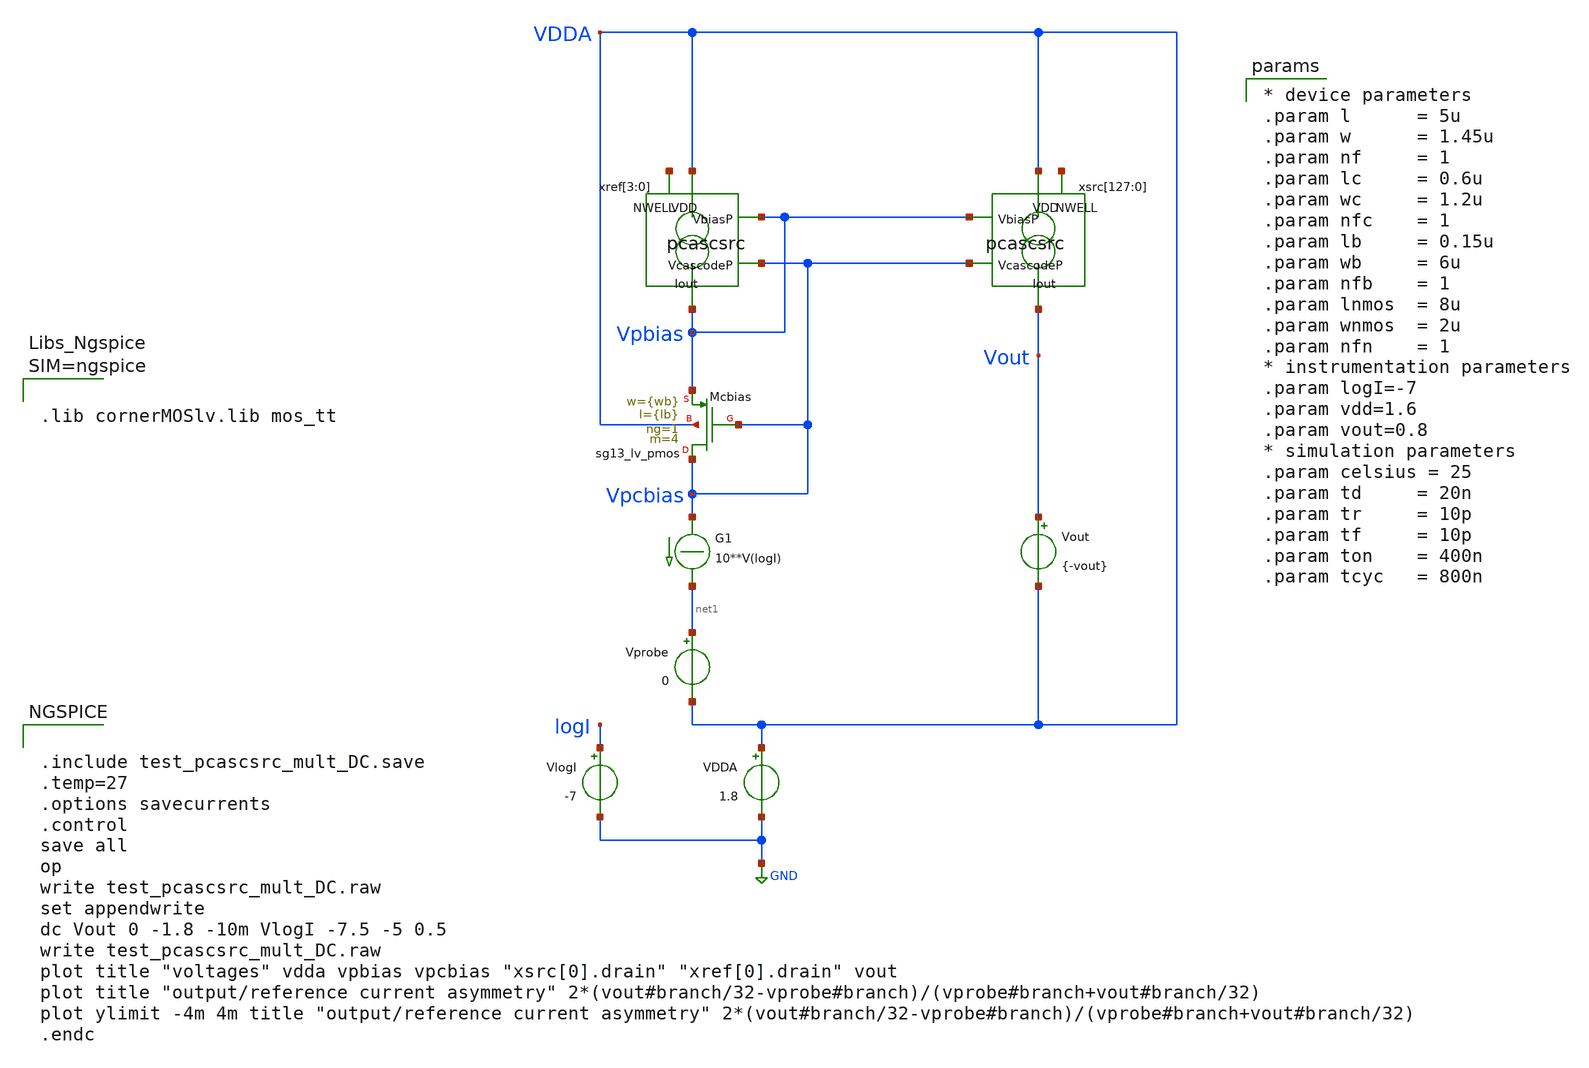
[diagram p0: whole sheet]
** sch_path: xschem/test_pcascsrc_mult_DC.sch
**.subckt test_pcascsrc_mult_DC
Vout Vout VDDA {-vout}
.save i(vout)
Vprobe net1 VDDA 0
.save i(vprobe)
G1 Vpcbias net1 CUR=' 10**V(logI) '
VlogI logI GND -7
.save i(vlogi)
xref[3] VDDA Vpbias Vpcbias Vpbias net2[3] pcascsrc
xref[2] VDDA Vpbias Vpcbias Vpbias net2[2] pcascsrc
xref[1] VDDA Vpbias Vpcbias Vpbias net2[1] pcascsrc
xref[0] VDDA Vpbias Vpcbias Vpbias net2[0] pcascsrc
xsrc[127] VDDA Vpbias Vpcbias Vout net3[127] pcascsrc
xsrc[126] VDDA Vpbias Vpcbias Vout net3[126] pcascsrc
xsrc[125] VDDA Vpbias Vpcbias Vout net3[125] pcascsrc
xsrc[124] VDDA Vpbias Vpcbias Vout net3[124] pcascsrc
xsrc[123] VDDA Vpbias Vpcbias Vout net3[123] pcascsrc
xsrc[122] VDDA Vpbias Vpcbias Vout net3[122] pcascsrc
xsrc[121] VDDA Vpbias Vpcbias Vout net3[121] pcascsrc
xsrc[120] VDDA Vpbias Vpcbias Vout net3[120] pcascsrc
xsrc[119] VDDA Vpbias Vpcbias Vout net3[119] pcascsrc
xsrc[118] VDDA Vpbias Vpcbias Vout net3[118] pcascsrc
xsrc[117] VDDA Vpbias Vpcbias Vout net3[117] pcascsrc
xsrc[116] VDDA Vpbias Vpcbias Vout net3[116] pcascsrc
xsrc[115] VDDA Vpbias Vpcbias Vout net3[115] pcascsrc
xsrc[114] VDDA Vpbias Vpcbias Vout net3[114] pcascsrc
xsrc[113] VDDA Vpbias Vpcbias Vout net3[113] pcascsrc
xsrc[112] VDDA Vpbias Vpcbias Vout net3[112] pcascsrc
xsrc[111] VDDA Vpbias Vpcbias Vout net3[111] pcascsrc
xsrc[110] VDDA Vpbias Vpcbias Vout net3[110] pcascsrc
xsrc[109] VDDA Vpbias Vpcbias Vout net3[109] pcascsrc
xsrc[108] VDDA Vpbias Vpcbias Vout net3[108] pcascsrc
xsrc[107] VDDA Vpbias Vpcbias Vout net3[107] pcascsrc
xsrc[106] VDDA Vpbias Vpcbias Vout net3[106] pcascsrc
xsrc[105] VDDA Vpbias Vpcbias Vout net3[105] pcascsrc
xsrc[104] VDDA Vpbias Vpcbias Vout net3[104] pcascsrc
xsrc[103] VDDA Vpbias Vpcbias Vout net3[103] pcascsrc
xsrc[102] VDDA Vpbias Vpcbias Vout net3[102] pcascsrc
xsrc[101] VDDA Vpbias Vpcbias Vout net3[101] pcascsrc
xsrc[100] VDDA Vpbias Vpcbias Vout net3[100] pcascsrc
xsrc[99] VDDA Vpbias Vpcbias Vout net3[99] pcascsrc
xsrc[98] VDDA Vpbias Vpcbias Vout net3[98] pcascsrc
xsrc[97] VDDA Vpbias Vpcbias Vout net3[97] pcascsrc
xsrc[96] VDDA Vpbias Vpcbias Vout net3[96] pcascsrc
xsrc[95] VDDA Vpbias Vpcbias Vout net3[95] pcascsrc
xsrc[94] VDDA Vpbias Vpcbias Vout net3[94] pcascsrc
xsrc[93] VDDA Vpbias Vpcbias Vout net3[93] pcascsrc
xsrc[92] VDDA Vpbias Vpcbias Vout net3[92] pcascsrc
xsrc[91] VDDA Vpbias Vpcbias Vout net3[91] pcascsrc
xsrc[90] VDDA Vpbias Vpcbias Vout net3[90] pcascsrc
xsrc[89] VDDA Vpbias Vpcbias Vout net3[89] pcascsrc
xsrc[88] VDDA Vpbias Vpcbias Vout net3[88] pcascsrc
xsrc[87] VDDA Vpbias Vpcbias Vout net3[87] pcascsrc
xsrc[86] VDDA Vpbias Vpcbias Vout net3[86] pcascsrc
xsrc[85] VDDA Vpbias Vpcbias Vout net3[85] pcascsrc
xsrc[84] VDDA Vpbias Vpcbias Vout net3[84] pcascsrc
xsrc[83] VDDA Vpbias Vpcbias Vout net3[83] pcascsrc
xsrc[82] VDDA Vpbias Vpcbias Vout net3[82] pcascsrc
xsrc[81] VDDA Vpbias Vpcbias Vout net3[81] pcascsrc
xsrc[80] VDDA Vpbias Vpcbias Vout net3[80] pcascsrc
xsrc[79] VDDA Vpbias Vpcbias Vout net3[79] pcascsrc
xsrc[78] VDDA Vpbias Vpcbias Vout net3[78] pcascsrc
xsrc[77] VDDA Vpbias Vpcbias Vout net3[77] pcascsrc
xsrc[76] VDDA Vpbias Vpcbias Vout net3[76] pcascsrc
xsrc[75] VDDA Vpbias Vpcbias Vout net3[75] pcascsrc
xsrc[74] VDDA Vpbias Vpcbias Vout net3[74] pcascsrc
xsrc[73] VDDA Vpbias Vpcbias Vout net3[73] pcascsrc
xsrc[72] VDDA Vpbias Vpcbias Vout net3[72] pcascsrc
xsrc[71] VDDA Vpbias Vpcbias Vout net3[71] pcascsrc
xsrc[70] VDDA Vpbias Vpcbias Vout net3[70] pcascsrc
xsrc[69] VDDA Vpbias Vpcbias Vout net3[69] pcascsrc
xsrc[68] VDDA Vpbias Vpcbias Vout net3[68] pcascsrc
xsrc[67] VDDA Vpbias Vpcbias Vout net3[67] pcascsrc
xsrc[66] VDDA Vpbias Vpcbias Vout net3[66] pcascsrc
xsrc[65] VDDA Vpbias Vpcbias Vout net3[65] pcascsrc
xsrc[64] VDDA Vpbias Vpcbias Vout net3[64] pcascsrc
xsrc[63] VDDA Vpbias Vpcbias Vout net3[63] pcascsrc
xsrc[62] VDDA Vpbias Vpcbias Vout net3[62] pcascsrc
xsrc[61] VDDA Vpbias Vpcbias Vout net3[61] pcascsrc
xsrc[60] VDDA Vpbias Vpcbias Vout net3[60] pcascsrc
xsrc[59] VDDA Vpbias Vpcbias Vout net3[59] pcascsrc
xsrc[58] VDDA Vpbias Vpcbias Vout net3[58] pcascsrc
xsrc[57] VDDA Vpbias Vpcbias Vout net3[57] pcascsrc
xsrc[56] VDDA Vpbias Vpcbias Vout net3[56] pcascsrc
xsrc[55] VDDA Vpbias Vpcbias Vout net3[55] pcascsrc
xsrc[54] VDDA Vpbias Vpcbias Vout net3[54] pcascsrc
xsrc[53] VDDA Vpbias Vpcbias Vout net3[53] pcascsrc
xsrc[52] VDDA Vpbias Vpcbias Vout net3[52] pcascsrc
xsrc[51] VDDA Vpbias Vpcbias Vout net3[51] pcascsrc
xsrc[50] VDDA Vpbias Vpcbias Vout net3[50] pcascsrc
xsrc[49] VDDA Vpbias Vpcbias Vout net3[49] pcascsrc
xsrc[48] VDDA Vpbias Vpcbias Vout net3[48] pcascsrc
xsrc[47] VDDA Vpbias Vpcbias Vout net3[47] pcascsrc
xsrc[46] VDDA Vpbias Vpcbias Vout net3[46] pcascsrc
xsrc[45] VDDA Vpbias Vpcbias Vout net3[45] pcascsrc
xsrc[44] VDDA Vpbias Vpcbias Vout net3[44] pcascsrc
xsrc[43] VDDA Vpbias Vpcbias Vout net3[43] pcascsrc
xsrc[42] VDDA Vpbias Vpcbias Vout net3[42] pcascsrc
xsrc[41] VDDA Vpbias Vpcbias Vout net3[41] pcascsrc
xsrc[40] VDDA Vpbias Vpcbias Vout net3[40] pcascsrc
xsrc[39] VDDA Vpbias Vpcbias Vout net3[39] pcascsrc
xsrc[38] VDDA Vpbias Vpcbias Vout net3[38] pcascsrc
xsrc[37] VDDA Vpbias Vpcbias Vout net3[37] pcascsrc
xsrc[36] VDDA Vpbias Vpcbias Vout net3[36] pcascsrc
xsrc[35] VDDA Vpbias Vpcbias Vout net3[35] pcascsrc
xsrc[34] VDDA Vpbias Vpcbias Vout net3[34] pcascsrc
xsrc[33] VDDA Vpbias Vpcbias Vout net3[33] pcascsrc
xsrc[32] VDDA Vpbias Vpcbias Vout net3[32] pcascsrc
xsrc[31] VDDA Vpbias Vpcbias Vout net3[31] pcascsrc
xsrc[30] VDDA Vpbias Vpcbias Vout net3[30] pcascsrc
xsrc[29] VDDA Vpbias Vpcbias Vout net3[29] pcascsrc
xsrc[28] VDDA Vpbias Vpcbias Vout net3[28] pcascsrc
xsrc[27] VDDA Vpbias Vpcbias Vout net3[27] pcascsrc
xsrc[26] VDDA Vpbias Vpcbias Vout net3[26] pcascsrc
xsrc[25] VDDA Vpbias Vpcbias Vout net3[25] pcascsrc
xsrc[24] VDDA Vpbias Vpcbias Vout net3[24] pcascsrc
xsrc[23] VDDA Vpbias Vpcbias Vout net3[23] pcascsrc
xsrc[22] VDDA Vpbias Vpcbias Vout net3[22] pcascsrc
xsrc[21] VDDA Vpbias Vpcbias Vout net3[21] pcascsrc
xsrc[20] VDDA Vpbias Vpcbias Vout net3[20] pcascsrc
xsrc[19] VDDA Vpbias Vpcbias Vout net3[19] pcascsrc
xsrc[18] VDDA Vpbias Vpcbias Vout net3[18] pcascsrc
xsrc[17] VDDA Vpbias Vpcbias Vout net3[17] pcascsrc
xsrc[16] VDDA Vpbias Vpcbias Vout net3[16] pcascsrc
xsrc[15] VDDA Vpbias Vpcbias Vout net3[15] pcascsrc
xsrc[14] VDDA Vpbias Vpcbias Vout net3[14] pcascsrc
xsrc[13] VDDA Vpbias Vpcbias Vout net3[13] pcascsrc
xsrc[12] VDDA Vpbias Vpcbias Vout net3[12] pcascsrc
xsrc[11] VDDA Vpbias Vpcbias Vout net3[11] pcascsrc
xsrc[10] VDDA Vpbias Vpcbias Vout net3[10] pcascsrc
xsrc[9] VDDA Vpbias Vpcbias Vout net3[9] pcascsrc
xsrc[8] VDDA Vpbias Vpcbias Vout net3[8] pcascsrc
xsrc[7] VDDA Vpbias Vpcbias Vout net3[7] pcascsrc
xsrc[6] VDDA Vpbias Vpcbias Vout net3[6] pcascsrc
xsrc[5] VDDA Vpbias Vpcbias Vout net3[5] pcascsrc
xsrc[4] VDDA Vpbias Vpcbias Vout net3[4] pcascsrc
xsrc[3] VDDA Vpbias Vpcbias Vout net3[3] pcascsrc
xsrc[2] VDDA Vpbias Vpcbias Vout net3[2] pcascsrc
xsrc[1] VDDA Vpbias Vpcbias Vout net3[1] pcascsrc
xsrc[0] VDDA Vpbias Vpcbias Vout net3[0] pcascsrc
VDDA VDDA GND 1.8
.save i(vdda)
XMcbias Vpcbias Vpcbias Vpbias VDDA sg13_lv_pmos w={wb} l={lb} ng=1 m=4 mm_ok=1
**** begin user architecture code


.include test_pcascsrc_mult_DC.save
.temp=27
.options savecurrents
.control
save all
op
write test_pcascsrc_mult_DC.raw
set appendwrite
dc Vout 0 -1.8 -10m VlogI -7.5 -5 0.5
write test_pcascsrc_mult_DC.raw
plot title "voltages" vdda vpbias vpcbias "xsrc[0].drain" "xref[0].drain" vout
plot title "output/reference current asymmetry"
+ 2*(vout#branch/32-vprobe#branch)/(vprobe#branch+vout#branch/32)
plot ylimit -4m 4m title "output/reference current asymmetry"
+ 2*(vout#branch/32-vprobe#branch)/(vprobe#branch+vout#branch/32)
.endc





.lib cornerMOSlv.lib mos_tt




* device parameters
.param l      = 5u
.param w      = 1.45u
.param nf     = 1
.param lc     = 0.6u
.param wc     = 1.2u
.param nfc    = 1
.param lb     = 0.15u
.param wb     = 6u
.param nfb    = 1
.param lnmos  = 8u
.param wnmos  = 2u
.param nfn    = 1
* instrumentation parameters
.param logI=-7
.param vdd=1.6
.param vout=0.8
* simulation parameters
.param celsius = 25
.param td     = 20n
.param tr     = 10p
.param tf     = 10p
.param ton    = 400n
.param tcyc   = 800n


**** end user architecture code
**.ends

* expanding   symbol:  pcascsrc.sym # of pins=5
** sym_path: xschem/pcascsrc.sym
** sch_path: xschem/pcascsrc.sch
.subckt pcascsrc VDD VbiasP VcascodeP Iout NWELL
*.ipin VcascodeP
*.ipin VbiasP
*.opin Iout
*.ipin VDD
*.iopin NWELL
XMsrc drain VbiasP VDD NWELL sg13_lv_pmos w=0.74u l=2u ng=1 m=1 mm_ok=1
XMcasc Iout VcascodeP drain NWELL sg13_lv_pmos w=0.3u l=0.3u ng=1 m=1 mm_ok=1
.ends

.GLOBAL GND
.end
